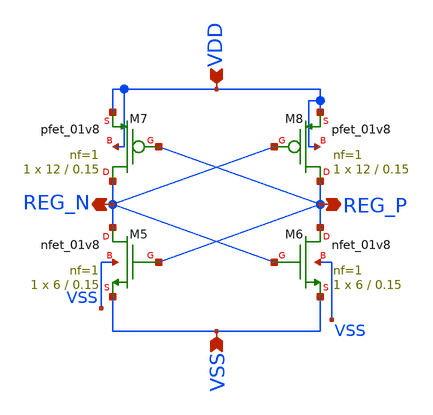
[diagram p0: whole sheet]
** sch_path: strongarm_core.sch
**.subckt strongarm_core VDD VSS REG_P REG_N
*.ipin VDD
*.ipin VSS
*.opin REG_P
*.opin REG_N
XM8 REG_P REG_N VDD VDD sky130_fd_pr__pfet_01v8 L=0.15 W=12 nf=1 ad='int((1 + 1)/2) * 12 / 1 * 0.29'
+ as='int((1 + 2)/2) * 12 / 1 * 0.29' pd='2*int((1 + 1)/2) * (12 / 1 + 0.29)' ps='2*int((1 + 2)/2) * (12 / 1 + 0.29)'
+ nrd='0.29 / 12 ' nrs='0.29 / 12 ' sa=0 sb=0 sd=0 mult=1 m=1
XM6 REG_P REG_N VSS VSS sky130_fd_pr__nfet_01v8 L=0.15 W=6 nf=1 ad='int((1 + 1)/2) * 6 / 1 * 0.29' as='int((1 + 2)/2) * 6 / 1 * 0.29'
+ pd='2*int((1 + 1)/2) * (6 / 1 + 0.29)' ps='2*int((1 + 2)/2) * (6 / 1 + 0.29)' nrd='0.29 / 6 ' nrs='0.29 / 6 '
+ sa=0 sb=0 sd=0 mult=1 m=1
XM5 REG_N REG_P VSS VSS sky130_fd_pr__nfet_01v8 L=0.15 W=6 nf=1 ad='int((1 + 1)/2) * 6 / 1 * 0.29' as='int((1 + 2)/2) * 6 / 1 * 0.29'
+ pd='2*int((1 + 1)/2) * (6 / 1 + 0.29)' ps='2*int((1 + 2)/2) * (6 / 1 + 0.29)' nrd='0.29 / 6 ' nrs='0.29 / 6 '
+ sa=0 sb=0 sd=0 mult=1 m=1
XM7 REG_N REG_P VDD VDD sky130_fd_pr__pfet_01v8 L=0.15 W=12 nf=1 ad='int((1 + 1)/2) * 12 / 1 * 0.29'
+ as='int((1 + 2)/2) * 12 / 1 * 0.29' pd='2*int((1 + 1)/2) * (12 / 1 + 0.29)' ps='2*int((1 + 2)/2) * (12 / 1 + 0.29)'
+ nrd='0.29 / 12 ' nrs='0.29 / 12 ' sa=0 sb=0 sd=0 mult=1 m=1
**** begin user architecture code

** opencircuitdesign pdks install
.lib $::SKYWATER_MODELS/sky130.lib.spice tt

**** end user architecture code
**.ends
.end
